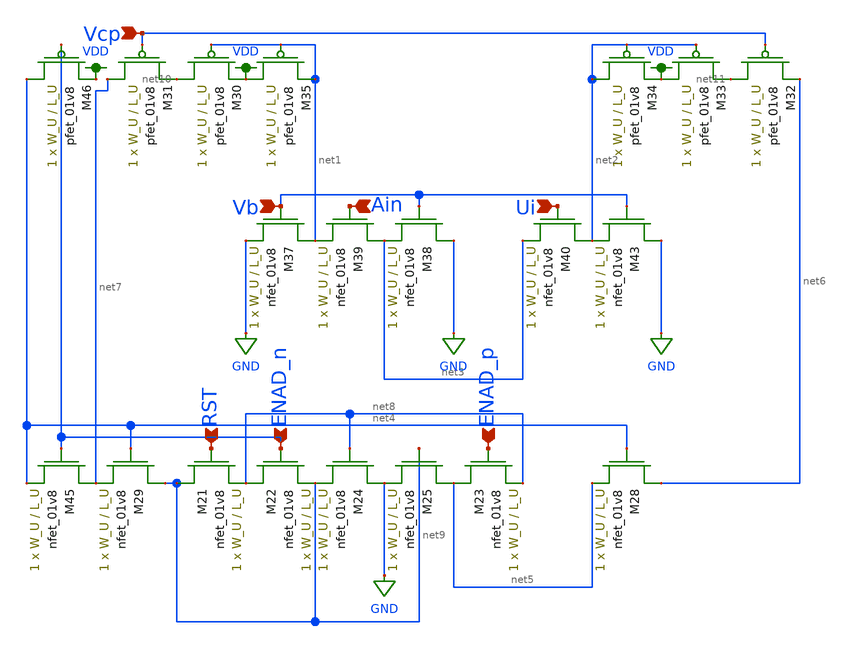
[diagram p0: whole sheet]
** sch_path: schematics/comp_lds.sch
**.subckt comp_lds RST ENAD_n ENAD_p Vcp Vb Ain Ui
*.ipin RST
*.ipin ENAD_n
*.ipin ENAD_p
*.ipin Vcp
*.ipin Vb
*.ipin Ain
*.ipin Ui
XM21 net9 RST net8 GND sky130_fd_pr__nfet_01v8 L=L_U W=W_U nf=1 ad='int((nf+1)/2) * W/nf * 0.29' as='int((nf+2)/2) * W/nf * 0.29'
+ pd='2*int((nf+1)/2) * (W/nf + 0.29)' ps='2*int((nf+2)/2) * (W/nf + 0.29)' nrd='0.29 / W' nrs='0.29 / W'
+ sa=0 sb=0 sd=0 mult=1 m=1
XM22 net8 ENAD_n net9 GND sky130_fd_pr__nfet_01v8 L=L_U W=W_U nf=1 ad='int((nf+1)/2) * W/nf * 0.29' as='int((nf+2)/2) * W/nf * 0.29'
+ pd='2*int((nf+1)/2) * (W/nf + 0.29)' ps='2*int((nf+2)/2) * (W/nf + 0.29)' nrd='0.29 / W' nrs='0.29 / W'
+ sa=0 sb=0 sd=0 mult=1 m=1
XM23 net5 ENAD_p net8 GND sky130_fd_pr__nfet_01v8 L=L_U W=W_U nf=1 ad='int((nf+1)/2) * W/nf * 0.29' as='int((nf+2)/2) * W/nf * 0.29'
+ pd='2*int((nf+1)/2) * (W/nf + 0.29)' ps='2*int((nf+2)/2) * (W/nf + 0.29)' nrd='0.29 / W' nrs='0.29 / W'
+ sa=0 sb=0 sd=0 mult=1 m=1
XM24 GND net8 net9 GND sky130_fd_pr__nfet_01v8 L=L_U W=W_U nf=1 ad='int((nf+1)/2) * W/nf * 0.29' as='int((nf+2)/2) * W/nf * 0.29'
+ pd='2*int((nf+1)/2) * (W/nf + 0.29)' ps='2*int((nf+2)/2) * (W/nf + 0.29)' nrd='0.29 / W' nrs='0.29 / W'
+ sa=0 sb=0 sd=0 mult=1 m=1
XM25 net5 net9 GND GND sky130_fd_pr__nfet_01v8 L=L_U W=W_U nf=1 ad='int((nf+1)/2) * W/nf * 0.29' as='int((nf+2)/2) * W/nf * 0.29'
+ pd='2*int((nf+1)/2) * (W/nf + 0.29)' ps='2*int((nf+2)/2) * (W/nf + 0.29)' nrd='0.29 / W' nrs='0.29 / W'
+ sa=0 sb=0 sd=0 mult=1 m=1
XM28 net6 net4 net5 GND sky130_fd_pr__nfet_01v8 L=L_U W=W_U nf=1 ad='int((nf+1)/2) * W/nf * 0.29' as='int((nf+2)/2) * W/nf * 0.29'
+ pd='2*int((nf+1)/2) * (W/nf + 0.29)' ps='2*int((nf+2)/2) * (W/nf + 0.29)' nrd='0.29 / W' nrs='0.29 / W'
+ sa=0 sb=0 sd=0 mult=1 m=1
XM29 net9 net4 net7 GND sky130_fd_pr__nfet_01v8 L=L_U W=W_U nf=1 ad='int((nf+1)/2) * W/nf * 0.29' as='int((nf+2)/2) * W/nf * 0.29'
+ pd='2*int((nf+1)/2) * (W/nf + 0.29)' ps='2*int((nf+2)/2) * (W/nf + 0.29)' nrd='0.29 / W' nrs='0.29 / W'
+ sa=0 sb=0 sd=0 mult=1 m=1
XM30 net10 net1 VDD VDD sky130_fd_pr__pfet_01v8 L=L_U W=W_U nf=1 ad='int((nf+1)/2) * W/nf * 0.29' as='int((nf+2)/2) * W/nf * 0.29'
+ pd='2*int((nf+1)/2) * (W/nf + 0.29)' ps='2*int((nf+2)/2) * (W/nf + 0.29)' nrd='0.29 / W' nrs='0.29 / W'
+ sa=0 sb=0 sd=0 mult=1 m=1
XM31 net7 Vcp net10 VDD sky130_fd_pr__pfet_01v8 L=L_U W=W_U nf=1 ad='int((nf+1)/2) * W/nf * 0.29' as='int((nf+2)/2) * W/nf * 0.29'
+ pd='2*int((nf+1)/2) * (W/nf + 0.29)' ps='2*int((nf+2)/2) * (W/nf + 0.29)' nrd='0.29 / W' nrs='0.29 / W'
+ sa=0 sb=0 sd=0 mult=1 m=1
XM32 net11 Vcp net6 VDD sky130_fd_pr__pfet_01v8 L=L_U W=W_U nf=1 ad='int((nf+1)/2) * W/nf * 0.29' as='int((nf+2)/2) * W/nf * 0.29'
+ pd='2*int((nf+1)/2) * (W/nf + 0.29)' ps='2*int((nf+2)/2) * (W/nf + 0.29)' nrd='0.29 / W' nrs='0.29 / W'
+ sa=0 sb=0 sd=0 mult=1 m=1
XM33 VDD net2 net11 VDD sky130_fd_pr__pfet_01v8 L=L_U W=W_U nf=1 ad='int((nf+1)/2) * W/nf * 0.29' as='int((nf+2)/2) * W/nf * 0.29'
+ pd='2*int((nf+1)/2) * (W/nf + 0.29)' ps='2*int((nf+2)/2) * (W/nf + 0.29)' nrd='0.29 / W' nrs='0.29 / W'
+ sa=0 sb=0 sd=0 mult=1 m=1
XM34 net2 net2 VDD VDD sky130_fd_pr__pfet_01v8 L=L_U W=W_U nf=1 ad='int((nf+1)/2) * W/nf * 0.29' as='int((nf+2)/2) * W/nf * 0.29'
+ pd='2*int((nf+1)/2) * (W/nf + 0.29)' ps='2*int((nf+2)/2) * (W/nf + 0.29)' nrd='0.29 / W' nrs='0.29 / W'
+ sa=0 sb=0 sd=0 mult=1 m=1
XM35 VDD net1 net1 VDD sky130_fd_pr__pfet_01v8 L=L_U W=W_U nf=1 ad='int((nf+1)/2) * W/nf * 0.29' as='int((nf+2)/2) * W/nf * 0.29'
+ pd='2*int((nf+1)/2) * (W/nf + 0.29)' ps='2*int((nf+2)/2) * (W/nf + 0.29)' nrd='0.29 / W' nrs='0.29 / W'
+ sa=0 sb=0 sd=0 mult=1 m=1
XM37 net1 Vb GND GND sky130_fd_pr__nfet_01v8 L=L_U W=W_U nf=1 ad='int((nf+1)/2) * W/nf * 0.29' as='int((nf+2)/2) * W/nf * 0.29'
+ pd='2*int((nf+1)/2) * (W/nf + 0.29)' ps='2*int((nf+2)/2) * (W/nf + 0.29)' nrd='0.29 / W' nrs='0.29 / W'
+ sa=0 sb=0 sd=0 mult=1 m=1
XM38 GND Vb net3 GND sky130_fd_pr__nfet_01v8 L=L_U W=W_U nf=1 ad='int((nf+1)/2) * W/nf * 0.29' as='int((nf+2)/2) * W/nf * 0.29'
+ pd='2*int((nf+1)/2) * (W/nf + 0.29)' ps='2*int((nf+2)/2) * (W/nf + 0.29)' nrd='0.29 / W' nrs='0.29 / W'
+ sa=0 sb=0 sd=0 mult=1 m=1
XM39 net3 Ain net1 GND sky130_fd_pr__nfet_01v8 L=L_U W=W_U nf=1 ad='int((nf+1)/2) * W/nf * 0.29' as='int((nf+2)/2) * W/nf * 0.29'
+ pd='2*int((nf+1)/2) * (W/nf + 0.29)' ps='2*int((nf+2)/2) * (W/nf + 0.29)' nrd='0.29 / W' nrs='0.29 / W'
+ sa=0 sb=0 sd=0 mult=1 m=1
XM40 net2 Ui net3 GND sky130_fd_pr__nfet_01v8 L=L_U W=W_U nf=1 ad='int((nf+1)/2) * W/nf * 0.29' as='int((nf+2)/2) * W/nf * 0.29'
+ pd='2*int((nf+1)/2) * (W/nf + 0.29)' ps='2*int((nf+2)/2) * (W/nf + 0.29)' nrd='0.29 / W' nrs='0.29 / W'
+ sa=0 sb=0 sd=0 mult=1 m=1
XM43 GND Vb net2 GND sky130_fd_pr__nfet_01v8 L=L_U W=W_U nf=1 ad='int((nf+1)/2) * W/nf * 0.29' as='int((nf+2)/2) * W/nf * 0.29'
+ pd='2*int((nf+1)/2) * (W/nf + 0.29)' ps='2*int((nf+2)/2) * (W/nf + 0.29)' nrd='0.29 / W' nrs='0.29 / W'
+ sa=0 sb=0 sd=0 mult=1 m=1
XM46 net4 ENAD_n VDD VDD sky130_fd_pr__pfet_01v8 L=L_U W=W_U nf=1 ad='int((nf+1)/2) * W/nf * 0.29' as='int((nf+2)/2) * W/nf * 0.29'
+ pd='2*int((nf+1)/2) * (W/nf + 0.29)' ps='2*int((nf+2)/2) * (W/nf + 0.29)' nrd='0.29 / W' nrs='0.29 / W'
+ sa=0 sb=0 sd=0 mult=1 m=1
XM45 net7 ENAD_n net4 GND sky130_fd_pr__nfet_01v8 L=L_U W=W_U nf=1 ad='int((nf+1)/2) * W/nf * 0.29' as='int((nf+2)/2) * W/nf * 0.29'
+ pd='2*int((nf+1)/2) * (W/nf + 0.29)' ps='2*int((nf+2)/2) * (W/nf + 0.29)' nrd='0.29 / W' nrs='0.29 / W'
+ sa=0 sb=0 sd=0 mult=1 m=1
**.ends
.GLOBAL GND
.GLOBAL VDD
.end
